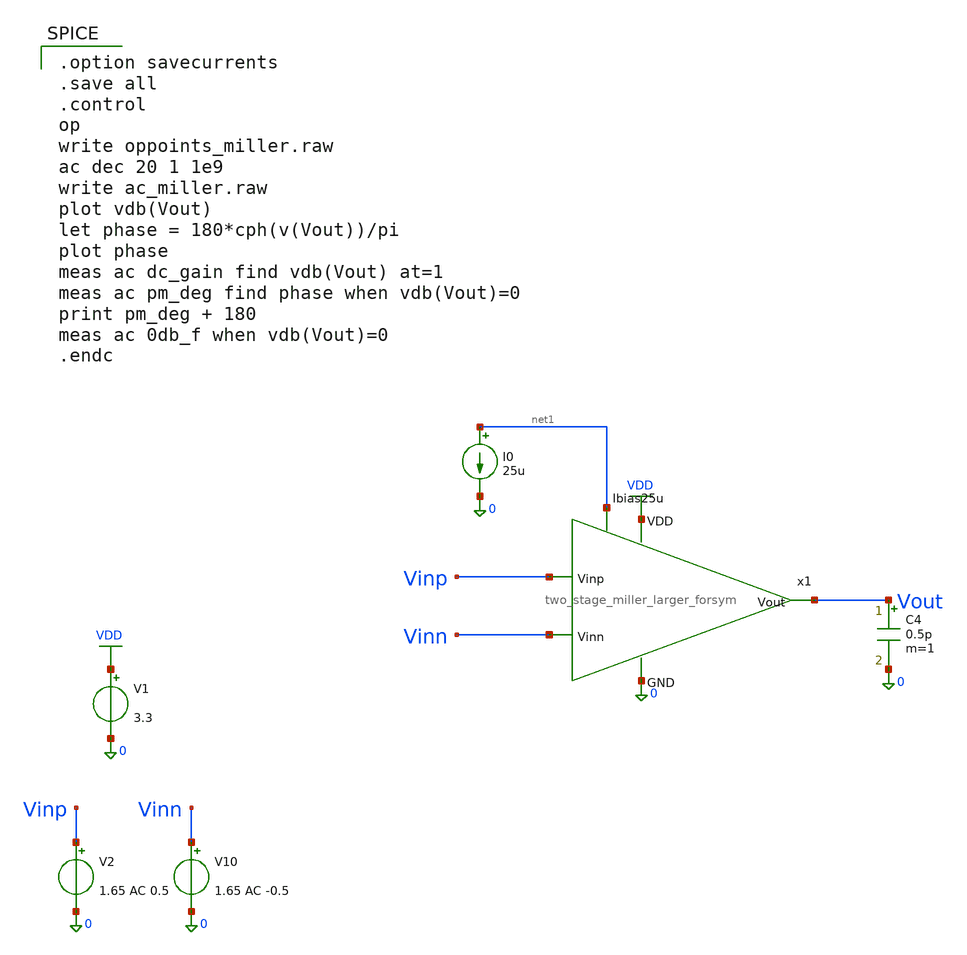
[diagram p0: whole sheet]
** sch_path: jz_tia/xschem/two_stage_miller_forsym_tb.sch
**.subckt two_stage_miller_forsym_tb
V2 Vinp 0 1.65 AC 0.5
V10 Vinn 0 1.65 AC -0.5
V1 VDD 0 3.3
I0 net1 0 25u
C4 Vout 0 0.5p m=1
x1 VDD Vout Vinp Vinn net1 0 two_stage_miller_larger_forsym
**** begin user architecture code

.include $::180MCU_MODELS/design.ngspice
.lib $::180MCU_MODELS/sm141064.ngspice typical
.lib $::180MCU_MODELS/smbb000149.ngspice typical


.option savecurrents
.save all
.control
op
write oppoints_miller.raw
ac dec 20 1 1e9
write ac_miller.raw
plot vdb(Vout)
let phase = 180*cph(v(Vout))/pi
plot phase
meas ac dc_gain find vdb(Vout) at=1
meas ac pm_deg find phase when vdb(Vout)=0
print pm_deg + 180
meas ac 0db_f when vdb(Vout)=0
.endc

**** end user architecture code
**.ends
.GLOBAL VDD
.end
